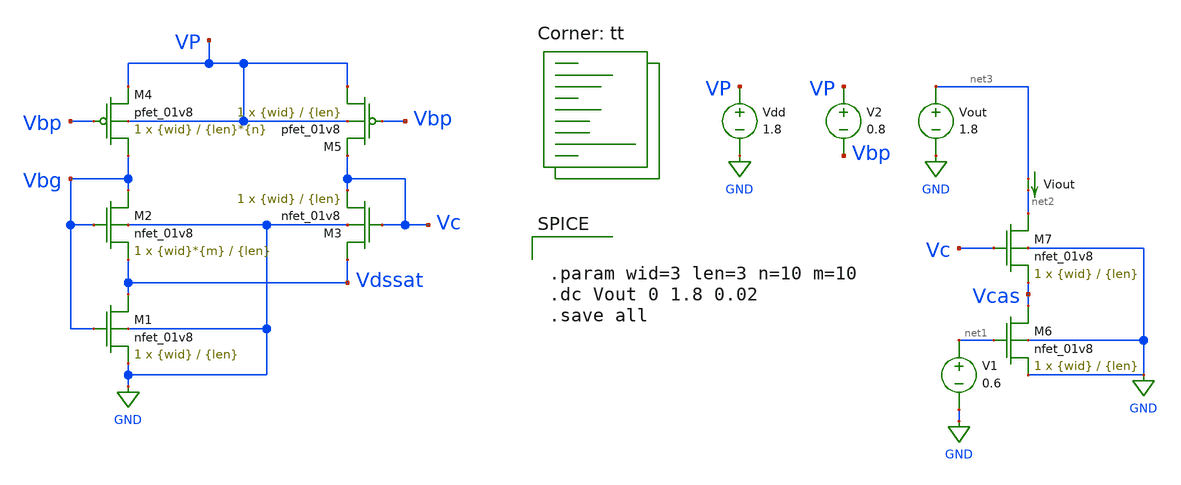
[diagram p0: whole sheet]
** sch_path: cbc.sch
**.subckt cbc
XM1 Vdssat Vbg GND GND sky130_fd_pr__nfet_01v8 L={len} W={wid} nf=1 ad='int((nf+1)/2) * W/nf * 0.29'
+ as='int((nf+2)/2) * W/nf * 0.29' pd='2*int((nf+1)/2) * (W/nf + 0.29)' ps='2*int((nf+2)/2) * (W/nf + 0.29)'
+ nrd='0.29 / W' nrs='0.29 / W' sa=0 sb=0 sd=0 mult=1 m=1
XM2 Vbg Vbg Vdssat GND sky130_fd_pr__nfet_01v8 L={len} W={wid}*{m} nf=1 ad='int((nf+1)/2) * W/nf * 0.29'
+ as='int((nf+2)/2) * W/nf * 0.29' pd='2*int((nf+1)/2) * (W/nf + 0.29)' ps='2*int((nf+2)/2) * (W/nf + 0.29)'
+ nrd='0.29 / W' nrs='0.29 / W' sa=0 sb=0 sd=0 mult=1 m=1
XM3 Vdssat Vc Vc GND sky130_fd_pr__nfet_01v8 L={len} W={wid} nf=1 ad='int((nf+1)/2) * W/nf * 0.29' as='int((nf+2)/2) * W/nf * 0.29'
+ pd='2*int((nf+1)/2) * (W/nf + 0.29)' ps='2*int((nf+2)/2) * (W/nf + 0.29)' nrd='0.29 / W' nrs='0.29 / W'
+ sa=0 sb=0 sd=0 mult=1 m=1
XM4 Vbg Vbp VP VP sky130_fd_pr__pfet_01v8 L={len}*{n} W={wid} nf=1 ad='int((nf+1)/2) * W/nf * 0.29' as='int((nf+2)/2) * W/nf * 0.29'
+ pd='2*int((nf+1)/2) * (W/nf + 0.29)' ps='2*int((nf+2)/2) * (W/nf + 0.29)' nrd='0.29 / W' nrs='0.29 / W'
+ sa=0 sb=0 sd=0 mult=1 m=1
XM5 VP Vbp Vc VP sky130_fd_pr__pfet_01v8 L={len} W={wid} nf=1 ad='int((nf+1)/2) * W/nf * 0.29' as='int((nf+2)/2) * W/nf * 0.29'
+ pd='2*int((nf+1)/2) * (W/nf + 0.29)' ps='2*int((nf+2)/2) * (W/nf + 0.29)' nrd='0.29 / W' nrs='0.29 / W'
+ sa=0 sb=0 sd=0 mult=1 m=1
Vdd VP GND 1.8
V2 VP Vbp 0.8
XM6 Vcas net1 GND GND sky130_fd_pr__nfet_01v8 L={len} W={wid} nf=1 ad='int((nf+1)/2) * W/nf * 0.29' as='int((nf+2)/2) * W/nf * 0.29'
+ pd='2*int((nf+1)/2) * (W/nf + 0.29)' ps='2*int((nf+2)/2) * (W/nf + 0.29)' nrd='0.29 / W' nrs='0.29 / W'
+ sa=0 sb=0 sd=0 mult=1 m=1
XM7 net2 Vc Vcas GND sky130_fd_pr__nfet_01v8 L={len} W={wid} nf=1 ad='int((nf+1)/2) * W/nf * 0.29' as='int((nf+2)/2) * W/nf * 0.29'
+ pd='2*int((nf+1)/2) * (W/nf + 0.29)' ps='2*int((nf+2)/2) * (W/nf + 0.29)' nrd='0.29 / W' nrs='0.29 / W'
+ sa=0 sb=0 sd=0 mult=1 m=1
V1 net1 GND 0.6
Viout net3 net2 0
.save i(viout)
Vout net3 GND 1.8
**** begin user architecture code


.param wid=3 len=3 n=10 m=10
.dc Vout 0 1.8 0.02
.save all


.lib $::SKYWATER_MODELS/sky130.lib.spice tt
**** end user architecture code
**.ends
.GLOBAL GND
.end
